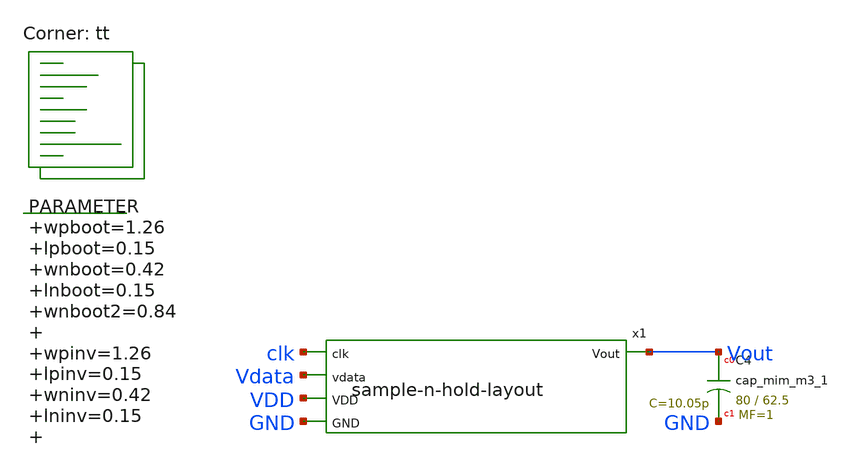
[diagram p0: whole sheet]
** sch_path: xschem/sample-n-hold-layout-tb.sch
**.subckt sample-n-hold-layout-tb
XC4 Vout GND sky130_fd_pr__cap_mim_m3_1 W=80 L=62.5 MF=1 m=1
.param wpboot=1.26 lpboot=0.15 wnboot=0.42 lnboot=0.15 wnboot2=0.84 wpinv=1.26 lpinv=0.15 wninv=0.42
+ lninv=0.15 wcboot=8 lcboot=6.25 wnsw=5 lnsw=0.3 wnsw2=1 wpsw=2


x1 clk Vdata VDD GND Vout sample-n-hold-layout
**** begin user architecture code
 .lib $::SKYWATER_MODELS/sky130.lib.spice tt
.include $::SKYWATER_STDCELLS/sky130_fd_sc_hd.spice
.param mc_mm_switch = 0
.param mc_pr_switch = 0




  .include ~/gits/UNIC-CASS-2024/spice/sample-n-hold-layout.spice
  .param fin=10e3
  .param fclk={fin*10} tclk={1/fclk} thclk={tclk/2}
  .option wnflag=1
  .option safecurrents

  Vvdd vdd   gnd 1.8
  Vdt  vdata gnd sin(0.5 0.5 9.3e3 10e-9)
  Vclk clk   gnd pulse(0 1.8 10e-9 1p 1p {thclk} {tclk})

  .control
    reset
    save all
    tran 10n 1m
    write sample-n-hold-circuit-tb.raw
    quit 0
  .endc



**** end user architecture code
**.ends
.end
